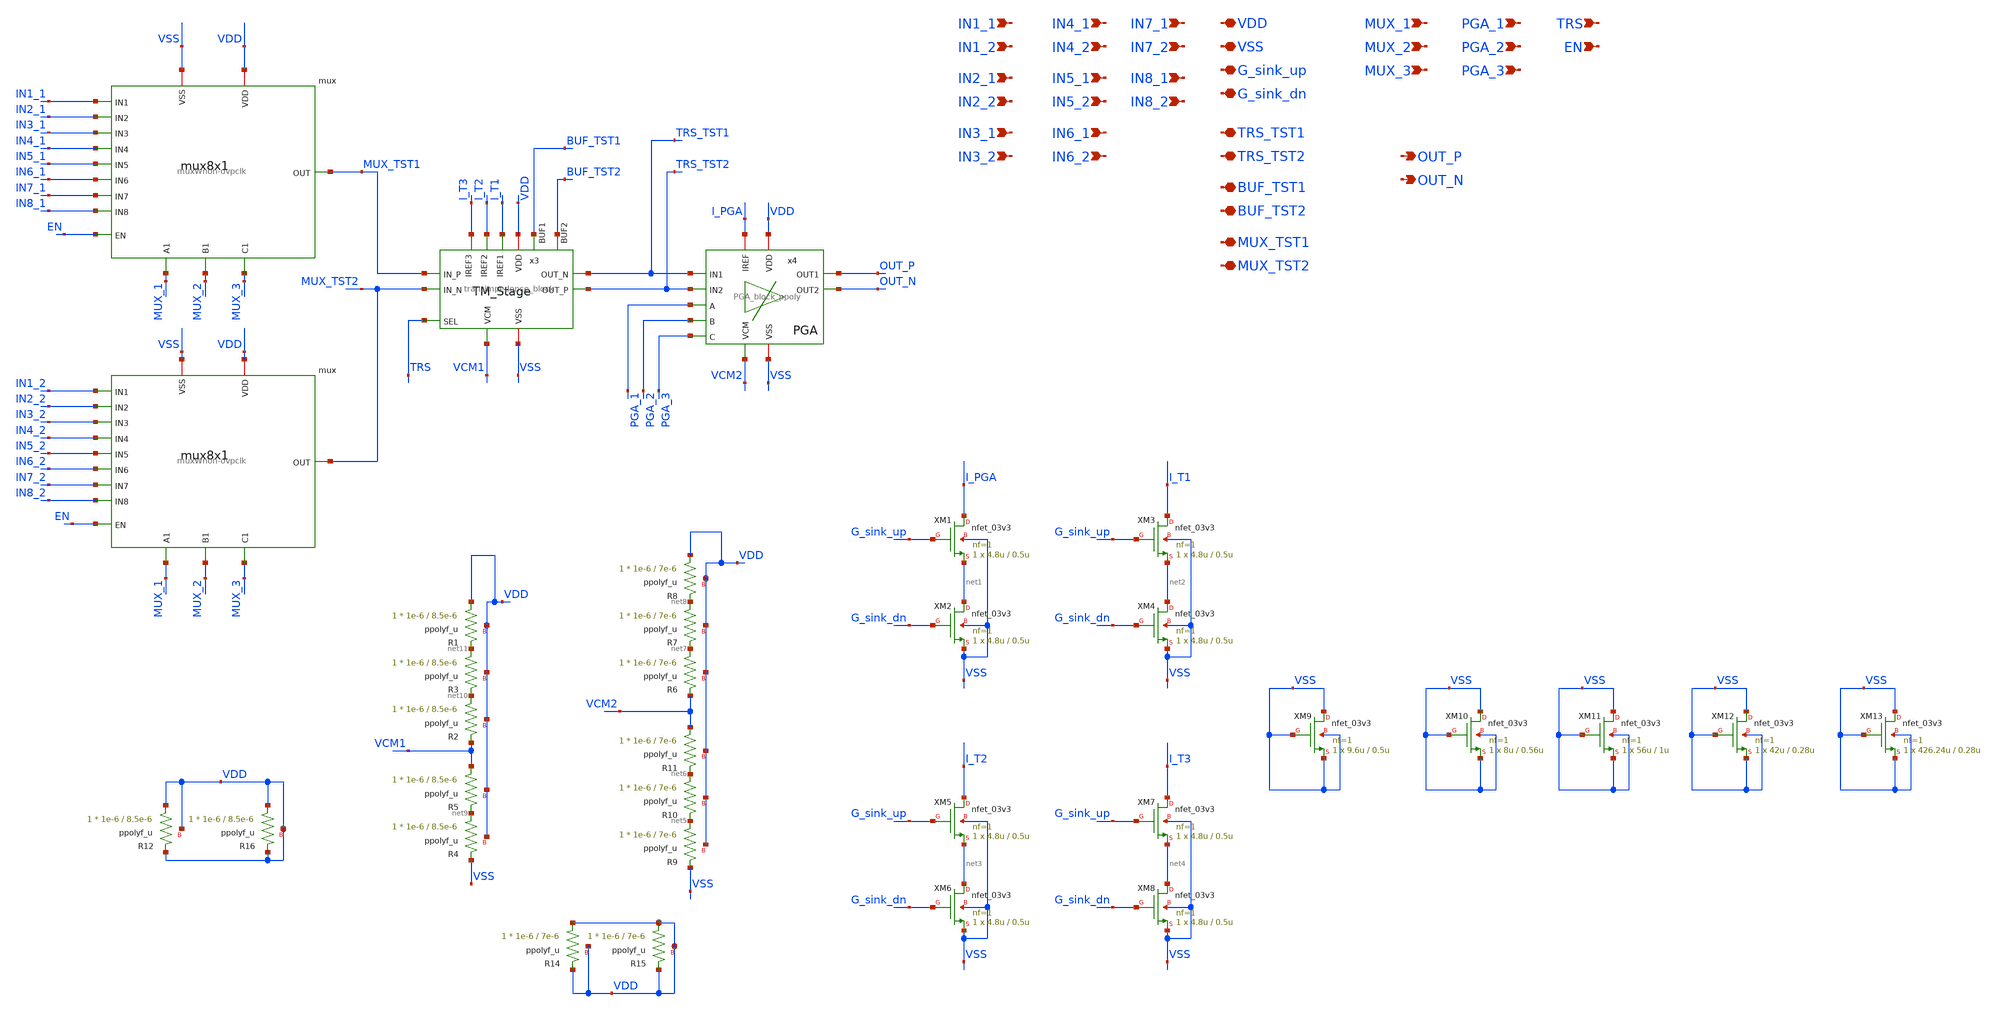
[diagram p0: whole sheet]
** sch_path: SCOP_INPUT_AND_MUX_PAKISTAN_03/Xschem/Complete_Design/comple_PICO_lvs.sch
**.subckt comple_PICO_lvs VDD VSS IN1_1 IN1_2 IN2_1 IN2_2 IN3_1 IN3_2 IN4_1 IN4_2 IN5_1 IN5_2 IN6_1
*+ IN6_2 IN7_1 IN7_2 IN8_1 IN8_2 G_sink_up G_sink_dn MUX_1 MUX_2 MUX_3 PGA_1 PGA_2 PGA_3 OUT_P OUT_N
*+ TRS_TST1 TRS_TST2 BUF_TST1 BUF_TST2 MUX_TST1 MUX_TST2 TRS EN
*.iopin VDD
*.iopin VSS
*.ipin IN1_1
*.ipin IN1_2
*.ipin IN2_1
*.ipin IN2_2
*.ipin IN3_1
*.ipin IN3_2
*.ipin IN4_1
*.ipin IN4_2
*.ipin IN5_1
*.ipin IN5_2
*.ipin IN6_1
*.ipin IN6_2
*.ipin IN7_1
*.ipin IN7_2
*.ipin IN8_1
*.ipin IN8_2
*.iopin G_sink_up
*.iopin G_sink_dn
*.ipin MUX_1
*.ipin MUX_2
*.ipin MUX_3
*.ipin PGA_1
*.ipin PGA_2
*.ipin PGA_3
*.opin OUT_P
*.opin OUT_N
*.iopin TRS_TST1
*.iopin TRS_TST2
*.iopin BUF_TST1
*.iopin BUF_TST2
*.iopin MUX_TST1
*.iopin MUX_TST2
*.ipin TRS
*.ipin EN
x1 VSS VDD IN1_1 IN2_1 IN3_1 MUX_2 IN4_1 MUX_TST1 IN5_1 MUX_3 IN6_1 IN7_1 IN8_1 MUX_1 EN
+ muxWnon-ovpclk
x2 VSS VDD IN1_2 IN2_2 IN3_2 MUX_2 IN4_2 MUX_TST2 IN5_2 MUX_3 IN6_2 IN7_2 IN8_2 MUX_1 EN
+ muxWnon-ovpclk
x3 MUX_TST1 MUX_TST2 TRS_TST1 VDD TRS_TST2 VSS I_T1 TRS VCM1 I_T2 I_T3 BUF_TST1 BUF_TST2
+ transimpedence_block
x4 TRS_TST1 TRS_TST2 OUT_P OUT_N VDD VSS I_PGA VCM2 PGA_1 PGA_2 PGA_3 PGA_block_ppoly
XM1 I_PGA G_sink_up net1 VSS nfet_03v3 L=0.5u W=4.8u nf=1 ad='int((nf+1)/2) * W/nf * 0.18u' as='int((nf+2)/2) * W/nf * 0.18u'
+ pd='2*int((nf+1)/2) * (W/nf + 0.18u)' ps='2*int((nf+2)/2) * (W/nf + 0.18u)' nrd='0.18u / W' nrs='0.18u / W'
+ sa=0 sb=0 sd=0 m=1
XM2 net1 G_sink_dn VSS VSS nfet_03v3 L=0.5u W=4.8u nf=1 ad='int((nf+1)/2) * W/nf * 0.18u' as='int((nf+2)/2) * W/nf * 0.18u'
+ pd='2*int((nf+1)/2) * (W/nf + 0.18u)' ps='2*int((nf+2)/2) * (W/nf + 0.18u)' nrd='0.18u / W' nrs='0.18u / W'
+ sa=0 sb=0 sd=0 m=1
XM3 I_T1 G_sink_up net2 VSS nfet_03v3 L=0.5u W=4.8u nf=1 ad='int((nf+1)/2) * W/nf * 0.18u' as='int((nf+2)/2) * W/nf * 0.18u'
+ pd='2*int((nf+1)/2) * (W/nf + 0.18u)' ps='2*int((nf+2)/2) * (W/nf + 0.18u)' nrd='0.18u / W' nrs='0.18u / W'
+ sa=0 sb=0 sd=0 m=1
XM4 net2 G_sink_dn VSS VSS nfet_03v3 L=0.5u W=4.8u nf=1 ad='int((nf+1)/2) * W/nf * 0.18u' as='int((nf+2)/2) * W/nf * 0.18u'
+ pd='2*int((nf+1)/2) * (W/nf + 0.18u)' ps='2*int((nf+2)/2) * (W/nf + 0.18u)' nrd='0.18u / W' nrs='0.18u / W'
+ sa=0 sb=0 sd=0 m=1
XM5 I_T2 G_sink_up net3 VSS nfet_03v3 L=0.5u W=4.8u nf=1 ad='int((nf+1)/2) * W/nf * 0.18u' as='int((nf+2)/2) * W/nf * 0.18u'
+ pd='2*int((nf+1)/2) * (W/nf + 0.18u)' ps='2*int((nf+2)/2) * (W/nf + 0.18u)' nrd='0.18u / W' nrs='0.18u / W'
+ sa=0 sb=0 sd=0 m=1
XM6 net3 G_sink_dn VSS VSS nfet_03v3 L=0.5u W=4.8u nf=1 ad='int((nf+1)/2) * W/nf * 0.18u' as='int((nf+2)/2) * W/nf * 0.18u'
+ pd='2*int((nf+1)/2) * (W/nf + 0.18u)' ps='2*int((nf+2)/2) * (W/nf + 0.18u)' nrd='0.18u / W' nrs='0.18u / W'
+ sa=0 sb=0 sd=0 m=1
XM7 I_T3 G_sink_up net4 VSS nfet_03v3 L=0.5u W=4.8u nf=1 ad='int((nf+1)/2) * W/nf * 0.18u' as='int((nf+2)/2) * W/nf * 0.18u'
+ pd='2*int((nf+1)/2) * (W/nf + 0.18u)' ps='2*int((nf+2)/2) * (W/nf + 0.18u)' nrd='0.18u / W' nrs='0.18u / W'
+ sa=0 sb=0 sd=0 m=1
XM8 net4 G_sink_dn VSS VSS nfet_03v3 L=0.5u W=4.8u nf=1 ad='int((nf+1)/2) * W/nf * 0.18u' as='int((nf+2)/2) * W/nf * 0.18u'
+ pd='2*int((nf+1)/2) * (W/nf + 0.18u)' ps='2*int((nf+2)/2) * (W/nf + 0.18u)' nrd='0.18u / W' nrs='0.18u / W'
+ sa=0 sb=0 sd=0 m=1
XM9 VSS VSS VSS VSS nfet_03v3 L=0.5u W=9.6u nf=1 ad='int((nf+1)/2) * W/nf * 0.18u' as='int((nf+2)/2) * W/nf * 0.18u'
+ pd='2*int((nf+1)/2) * (W/nf + 0.18u)' ps='2*int((nf+2)/2) * (W/nf + 0.18u)' nrd='0.18u / W' nrs='0.18u / W'
+ sa=0 sb=0 sd=0 m=1
XR16 VDD VDD VDD ppolyf_u r_width=1e-6 r_length=8.5e-6 m=1
XR14 VDD VDD VDD ppolyf_u r_width=1e-6 r_length=7e-6 m=1
XR15 VDD VDD VDD ppolyf_u r_width=1e-6 r_length=7e-6 m=1
XR9 net5 VSS VDD ppolyf_u r_width=1e-6 r_length=7e-6 m=1
XR10 net6 net5 VDD ppolyf_u r_width=1e-6 r_length=7e-6 m=1
XR11 VCM2 net6 VDD ppolyf_u r_width=1e-6 r_length=7e-6 m=1
XR6 net7 VCM2 VDD ppolyf_u r_width=1e-6 r_length=7e-6 m=1
XR7 net8 net7 VDD ppolyf_u r_width=1e-6 r_length=7e-6 m=1
XR8 VDD net8 VDD ppolyf_u r_width=1e-6 r_length=7e-6 m=1
XR12 VDD VDD VDD ppolyf_u r_width=1e-6 r_length=8.5e-6 m=1
XR4 net9 VSS VDD ppolyf_u r_width=1e-6 r_length=8.5e-6 m=1
XR5 VCM1 net9 VDD ppolyf_u r_width=1e-6 r_length=8.5e-6 m=1
XR2 net10 VCM1 VDD ppolyf_u r_width=1e-6 r_length=8.5e-6 m=1
XR3 net11 net10 VDD ppolyf_u r_width=1e-6 r_length=8.5e-6 m=1
XR1 VDD net11 VDD ppolyf_u r_width=1e-6 r_length=8.5e-6 m=1
XM10 VSS VSS VSS VSS nfet_03v3 L=0.56u W=8u nf=1 ad='int((nf+1)/2) * W/nf * 0.18u' as='int((nf+2)/2) * W/nf * 0.18u'
+ pd='2*int((nf+1)/2) * (W/nf + 0.18u)' ps='2*int((nf+2)/2) * (W/nf + 0.18u)' nrd='0.18u / W' nrs='0.18u / W'
+ sa=0 sb=0 sd=0 m=1
XM11 VSS VSS VSS VSS nfet_03v3 L=1u W=56u nf=1 ad='int((nf+1)/2) * W/nf * 0.18u' as='int((nf+2)/2) * W/nf * 0.18u'
+ pd='2*int((nf+1)/2) * (W/nf + 0.18u)' ps='2*int((nf+2)/2) * (W/nf + 0.18u)' nrd='0.18u / W' nrs='0.18u / W'
+ sa=0 sb=0 sd=0 m=1
XM12 VSS VSS VSS VSS nfet_03v3 L=0.28u W=42u nf=1 ad='int((nf+1)/2) * W/nf * 0.18u' as='int((nf+2)/2) * W/nf * 0.18u'
+ pd='2*int((nf+1)/2) * (W/nf + 0.18u)' ps='2*int((nf+2)/2) * (W/nf + 0.18u)' nrd='0.18u / W' nrs='0.18u / W'
+ sa=0 sb=0 sd=0 m=1
XM13 VSS VSS VSS VSS nfet_03v3 L=0.28u W=426.24u nf=1 ad='int((nf+1)/2) * W/nf * 0.18u' as='int((nf+2)/2) * W/nf * 0.18u'
+ pd='2*int((nf+1)/2) * (W/nf + 0.18u)' ps='2*int((nf+2)/2) * (W/nf + 0.18u)' nrd='0.18u / W' nrs='0.18u / W'
+ sa=0 sb=0 sd=0 m=1
**.ends
.end
